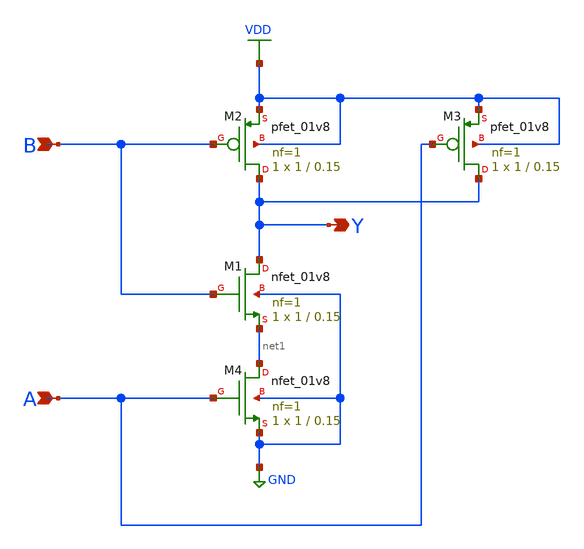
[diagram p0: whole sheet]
** sch_path: library/xschem/nand2.sch
**.subckt nand2 Y A B
*.opin Y
*.ipin A
*.ipin B
XM1 Y B net1 GND sky130_fd_pr__nfet_01v8 L=0.15 W=1 nf=1 ad='int((nf+1)/2) * W/nf * 0.29' as='int((nf+2)/2) * W/nf * 0.29'
+ pd='2*int((nf+1)/2) * (W/nf + 0.29)' ps='2*int((nf+2)/2) * (W/nf + 0.29)' nrd='0.29 / W' nrs='0.29 / W'
+ sa=0 sb=0 sd=0 mult=1 m=1
XM2 Y B VDD VDD sky130_fd_pr__pfet_01v8 L=0.15 W=1 nf=1 ad='int((nf+1)/2) * W/nf * 0.29' as='int((nf+2)/2) * W/nf * 0.29'
+ pd='2*int((nf+1)/2) * (W/nf + 0.29)' ps='2*int((nf+2)/2) * (W/nf + 0.29)' nrd='0.29 / W' nrs='0.29 / W'
+ sa=0 sb=0 sd=0 mult=1 m=1
XM3 Y A VDD VDD sky130_fd_pr__pfet_01v8 L=0.15 W=1 nf=1 ad='int((nf+1)/2) * W/nf * 0.29' as='int((nf+2)/2) * W/nf * 0.29'
+ pd='2*int((nf+1)/2) * (W/nf + 0.29)' ps='2*int((nf+2)/2) * (W/nf + 0.29)' nrd='0.29 / W' nrs='0.29 / W'
+ sa=0 sb=0 sd=0 mult=1 m=1
XM4 net1 A GND GND sky130_fd_pr__nfet_01v8 L=0.15 W=1 nf=1 ad='int((nf+1)/2) * W/nf * 0.29' as='int((nf+2)/2) * W/nf * 0.29'
+ pd='2*int((nf+1)/2) * (W/nf + 0.29)' ps='2*int((nf+2)/2) * (W/nf + 0.29)' nrd='0.29 / W' nrs='0.29 / W'
+ sa=0 sb=0 sd=0 mult=1 m=1
**.ends
.GLOBAL VDD
.GLOBAL GND
.end
